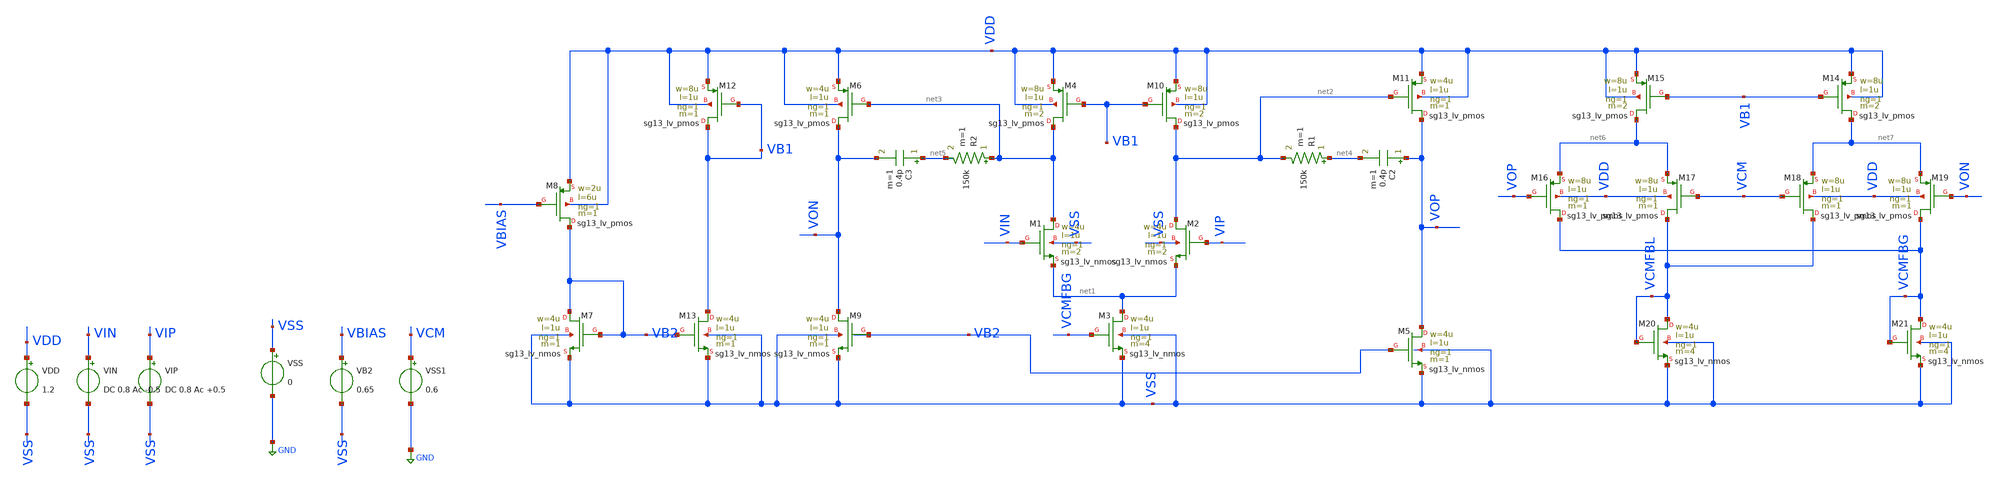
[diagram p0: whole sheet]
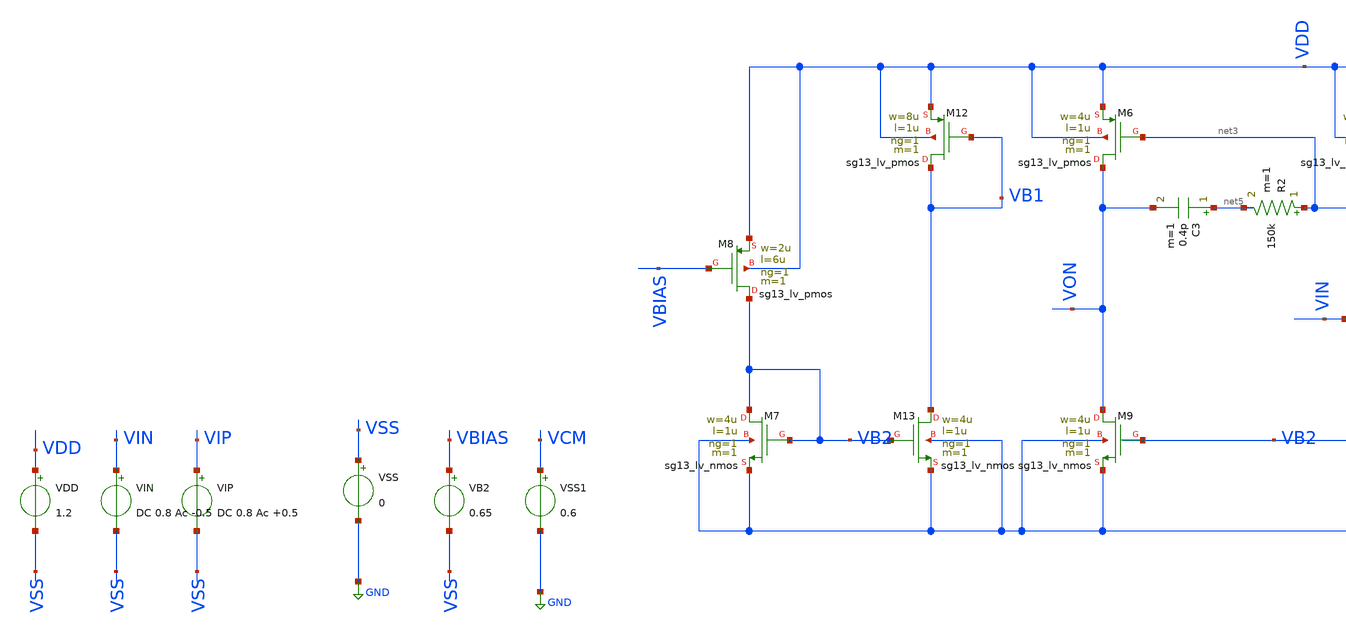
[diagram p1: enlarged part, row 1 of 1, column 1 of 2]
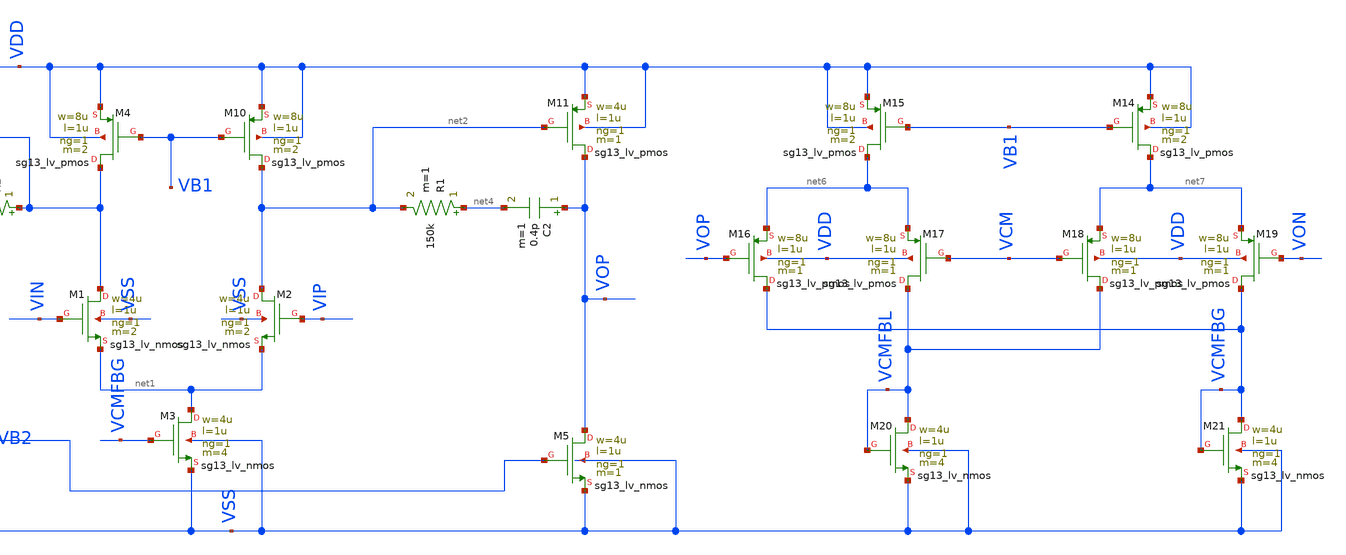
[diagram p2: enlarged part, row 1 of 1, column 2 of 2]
** sch_path: BTDay5-Ex/Ex3_6_Lecture5.sch
**.subckt Ex3_6_Lecture5
XM1 net3 VIN net1 VSS sg13_lv_nmos w=4u l=1u ng=1 m=2 mm_ok=1
XM2 net2 VIP net1 VSS sg13_lv_nmos w=4u l=1u ng=1 m=2 mm_ok=1
XM3 net1 VCMFBG VSS VSS sg13_lv_nmos w=4u l=1u ng=1 m=4 mm_ok=1
VDD VDD VSS 1.2
VIN VIN VSS DC 0.8 Ac -0.5
VIP VIP VSS DC 0.8 Ac +0.5
VSS VSS GND 0
XM4 net3 VB1 VDD VDD sg13_lv_pmos w=8u l=1u ng=1 m=2 mm_ok=1
XM7 VB2 VB2 VSS VSS sg13_lv_nmos w=4u l=1u ng=1 m=1 mm_ok=1
XM8 VB2 VBIAS VDD VDD sg13_lv_pmos w=2u l=6u ng=1 m=1 mm_ok=1
XM10 net2 VB1 VDD VDD sg13_lv_pmos w=8u l=1u ng=1 m=2 mm_ok=1
VB2 VBIAS VSS 0.65
XM5 VOP VB2 VSS VSS sg13_lv_nmos w=4u l=1u ng=1 m=1 mm_ok=1
XM11 VOP net2 VDD VDD sg13_lv_pmos w=4u l=1u ng=1 m=1 mm_ok=1
C2 VOP net4 0.4p m=1
R1 net4 net2 150k m=1
XM9 VON VB2 VSS VSS sg13_lv_nmos w=4u l=1u ng=1 m=1 mm_ok=1
C3 net5 VON 0.4p m=1
R2 net3 net5 150k m=1
XM12 VB1 VB1 VDD VDD sg13_lv_pmos w=8u l=1u ng=1 m=1 mm_ok=1
XM13 VB1 VB2 VSS VSS sg13_lv_nmos w=4u l=1u ng=1 m=1 mm_ok=1
XM6 VON net3 VDD VDD sg13_lv_pmos w=4u l=1u ng=1 m=1 mm_ok=1
XM14 net7 VB1 VDD VDD sg13_lv_pmos w=8u l=1u ng=1 m=2 mm_ok=1
XM15 net6 VB1 VDD VDD sg13_lv_pmos w=8u l=1u ng=1 m=2 mm_ok=1
XM16 VCMFBG VOP net6 VDD sg13_lv_pmos w=8u l=1u ng=1 m=1 mm_ok=1
XM17 VCMFBL VCM net6 VDD sg13_lv_pmos w=8u l=1u ng=1 m=1 mm_ok=1
XM18 VCMFBL VCM net7 VDD sg13_lv_pmos w=8u l=1u ng=1 m=1 mm_ok=1
XM19 VCMFBG VON net7 VDD sg13_lv_pmos w=8u l=1u ng=1 m=1 mm_ok=1
XM20 VCMFBL VCMFBL VSS VSS sg13_lv_nmos w=4u l=1u ng=1 m=4 mm_ok=1
XM21 VCMFBG VCMFBG VSS VSS sg13_lv_nmos w=4u l=1u ng=1 m=4 mm_ok=1
VSS1 VCM GND 0.6
**** begin user architecture code


.lib cornerMOSlv.lib mos_tt




.control

*==================================================
* 1. SAVE OPERATING-POINT PARAMETERS
*==================================================

save all

* NMOS
save @n.xm1.nsg13_lv_nmos[ids] @n.xm1.nsg13_lv_nmos[vgs] @n.xm1.nsg13_lv_nmos[vth]
+ @n.xm1.nsg13_lv_nmos[vds] @n.xm1.nsg13_lv_nmos[vdss] @n.xm1.nsg13_lv_nmos[gm] @n.xm1.nsg13_lv_nmos[gds]

save @n.xm2.nsg13_lv_nmos[ids] @n.xm2.nsg13_lv_nmos[vgs] @n.xm2.nsg13_lv_nmos[vth]
+ @n.xm2.nsg13_lv_nmos[vds] @n.xm2.nsg13_lv_nmos[vdss] @n.xm2.nsg13_lv_nmos[gm] @n.xm2.nsg13_lv_nmos[gds]

save @n.xm3.nsg13_lv_nmos[ids] @n.xm3.nsg13_lv_nmos[vgs] @n.xm3.nsg13_lv_nmos[vth]
+ @n.xm3.nsg13_lv_nmos[vds] @n.xm3.nsg13_lv_nmos[vdss] @n.xm3.nsg13_lv_nmos[gm] @n.xm3.nsg13_lv_nmos[gds]

save @n.xm5.nsg13_lv_nmos[ids] @n.xm5.nsg13_lv_nmos[vgs] @n.xm5.nsg13_lv_nmos[vth]
+ @n.xm5.nsg13_lv_nmos[vds] @n.xm5.nsg13_lv_nmos[vdss] @n.xm5.nsg13_lv_nmos[gm] @n.xm5.nsg13_lv_nmos[gds]

save @n.xm7.nsg13_lv_nmos[ids] @n.xm7.nsg13_lv_nmos[vgs] @n.xm7.nsg13_lv_nmos[vth]
+ @n.xm7.nsg13_lv_nmos[vds] @n.xm7.nsg13_lv_nmos[vdss] @n.xm7.nsg13_lv_nmos[gm] @n.xm7.nsg13_lv_nmos[gds]

* PMOS
save @n.xm4.nsg13_lv_pmos[ids] @n.xm4.nsg13_lv_pmos[vgs] @n.xm4.nsg13_lv_pmos[vth]
+ @n.xm4.nsg13_lv_pmos[vds] @n.xm4.nsg13_lv_pmos[vdss] @n.xm4.nsg13_lv_pmos[gm] @n.xm4.nsg13_lv_pmos[gds]

save @n.xm8.nsg13_lv_pmos[ids] @n.xm8.nsg13_lv_pmos[vgs] @n.xm8.nsg13_lv_pmos[vth]
+ @n.xm8.nsg13_lv_pmos[vds] @n.xm8.nsg13_lv_pmos[vdss] @n.xm8.nsg13_lv_pmos[gm] @n.xm8.nsg13_lv_pmos[gds]

save @n.xm10.nsg13_lv_pmos[ids] @n.xm10.nsg13_lv_pmos[vgs] @n.xm10.nsg13_lv_pmos[vth]
+ @n.xm10.nsg13_lv_pmos[vds] @n.xm10.nsg13_lv_pmos[vdss] @n.xm10.nsg13_lv_pmos[gm] @n.xm10.nsg13_lv_pmos[gds]

save @n.xm11.nsg13_lv_pmos[ids] @n.xm11.nsg13_lv_pmos[vgs] @n.xm11.nsg13_lv_pmos[vth]
+ @n.xm11.nsg13_lv_pmos[vds] @n.xm11.nsg13_lv_pmos[vdss] @n.xm11.nsg13_lv_pmos[gm] @n.xm11.nsg13_lv_pmos[gds]


*==================================================
* 2. DC OPERATING POINT
*==================================================

op

echo ================= M1 NMOS =================
print @n.xm1.nsg13_lv_nmos[vgs] @n.xm1.nsg13_lv_nmos[vth] @n.xm1.nsg13_lv_nmos[vds]
+ @n.xm1.nsg13_lv_nmos[vdss] @n.xm1.nsg13_lv_nmos[ids] @n.xm1.nsg13_lv_nmos[gm] @n.xm1.nsg13_lv_nmos[gds]

echo ================= M2 NMOS =================
print @n.xm2.nsg13_lv_nmos[vgs] @n.xm2.nsg13_lv_nmos[vth] @n.xm2.nsg13_lv_nmos[vds]
+ @n.xm2.nsg13_lv_nmos[vdss] @n.xm2.nsg13_lv_nmos[ids] @n.xm2.nsg13_lv_nmos[gm] @n.xm2.nsg13_lv_nmos[gds]

echo ================= M3 NMOS =================
print @n.xm3.nsg13_lv_nmos[vgs] @n.xm3.nsg13_lv_nmos[vth] @n.xm3.nsg13_lv_nmos[vds]
+ @n.xm3.nsg13_lv_nmos[vdss] @n.xm3.nsg13_lv_nmos[ids] @n.xm3.nsg13_lv_nmos[gm] @n.xm3.nsg13_lv_nmos[gds]

echo ================= M5 NMOS =================
print @n.xm5.nsg13_lv_nmos[vgs] @n.xm5.nsg13_lv_nmos[vth] @n.xm5.nsg13_lv_nmos[vds]
+ @n.xm5.nsg13_lv_nmos[vdss] @n.xm5.nsg13_lv_nmos[ids] @n.xm5.nsg13_lv_nmos[gm] @n.xm5.nsg13_lv_nmos[gds]

echo ================= M7 NMOS =================
print @n.xm7.nsg13_lv_nmos[vgs] @n.xm7.nsg13_lv_nmos[vth] @n.xm7.nsg13_lv_nmos[vds]
+ @n.xm7.nsg13_lv_nmos[vdss] @n.xm7.nsg13_lv_nmos[ids] @n.xm7.nsg13_lv_nmos[gm] @n.xm7.nsg13_lv_nmos[gds]

echo ================= M4 PMOS =================
print @n.xm4.nsg13_lv_pmos[vgs] @n.xm4.nsg13_lv_pmos[vth] @n.xm4.nsg13_lv_pmos[vds]
+ @n.xm4.nsg13_lv_pmos[vdss] @n.xm4.nsg13_lv_pmos[ids] @n.xm4.nsg13_lv_pmos[gm] @n.xm4.nsg13_lv_pmos[gds]

echo ================= M8 PMOS =================
print @n.xm8.nsg13_lv_pmos[vgs] @n.xm8.nsg13_lv_pmos[vth] @n.xm8.nsg13_lv_pmos[vds]
+ @n.xm8.nsg13_lv_pmos[vdss] @n.xm8.nsg13_lv_pmos[ids] @n.xm8.nsg13_lv_pmos[gm] @n.xm8.nsg13_lv_pmos[gds]

echo ================= M10 PMOS ================
print @n.xm10.nsg13_lv_pmos[vgs] @n.xm10.nsg13_lv_pmos[vth] @n.xm10.nsg13_lv_pmos[vds]
+ @n.xm10.nsg13_lv_pmos[vdss] @n.xm10.nsg13_lv_pmos[ids] @n.xm10.nsg13_lv_pmos[gm] @n.xm10.nsg13_lv_pmos[gds]

echo ================= M11 PMOS ================
print @n.xm11.nsg13_lv_pmos[vgs] @n.xm11.nsg13_lv_pmos[vth] @n.xm11.nsg13_lv_pmos[vds]
+ @n.xm11.nsg13_lv_pmos[vdss] @n.xm11.nsg13_lv_pmos[ids] @n.xm11.nsg13_lv_pmos[gm] @n.xm11.nsg13_lv_pmos[gds]

print v(vop) v(von)
print v(vg11) v(vg6)
print v(vb1) v(vb2)


write op_operating_point.raw

*==================================================
* 3. DIFFERENTIAL AC GAIN AND PHASE
*==================================================

ac dec 200 1 10G

let vid = v(vip)-v(vin)
let vod = v(vop)-v(von)
let av_diff = vod/vid

let gain_db = db(av_diff)
let phase_deg = cph(av_diff)*180/pi

if phase_deg[0] > 90
    let phase_deg = phase_deg-360
end

plot gain_db phase_deg xlog ylimit -360 80 title Differential

**** end user architecture code
**.ends
.GLOBAL GND
.end
